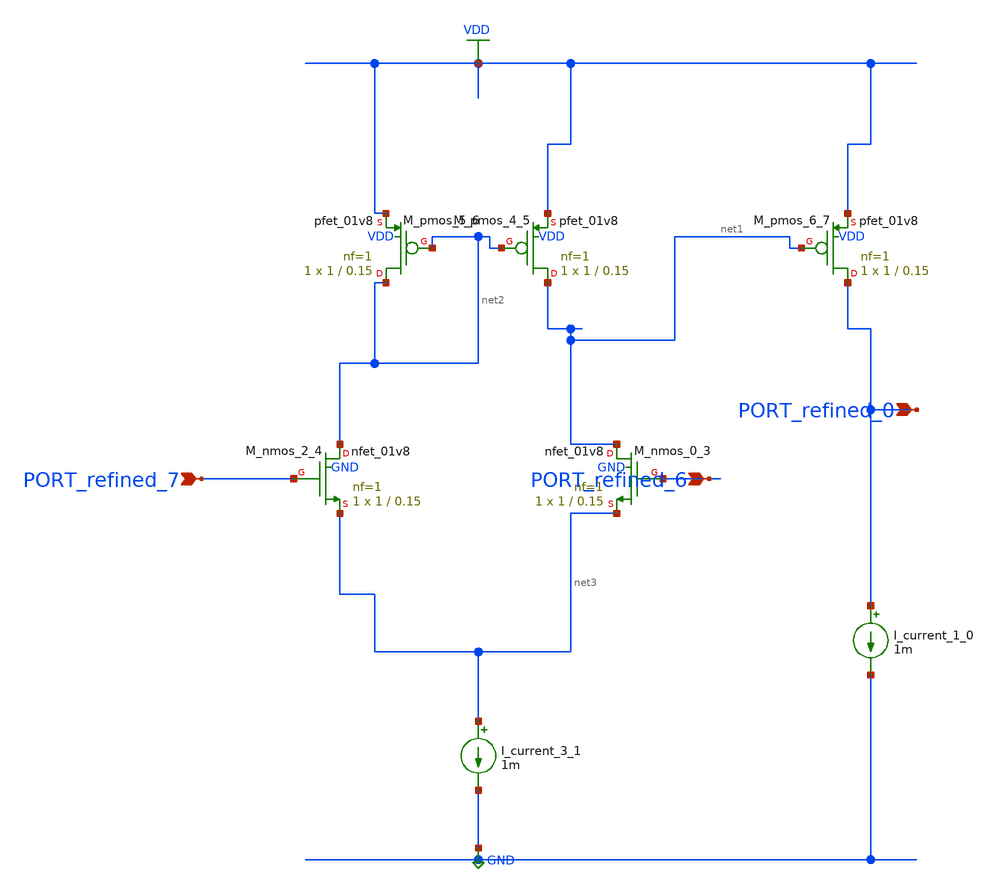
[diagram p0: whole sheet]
** sch_path: schematics/Image2Net/112.sch
**.subckt 112 PORT_refined_0 PORT_refined_6 PORT_refined_7
*.ipin PORT_refined_0
*.ipin PORT_refined_6
*.ipin PORT_refined_7
I_current_1_0 PORT_refined_0 GND 1m
I_current_3_1 net3 GND 1m
XM_nmos_0_3 net1 PORT_refined_6 net3 GND sky130_fd_pr__nfet_01v8 L=0.15 W=1 nf=1 ad='int((1 + 1)/2) * 1 / 1 * 0.29'
+ as='int((1 + 2)/2) * 1 / 1 * 0.29' pd='2*int((1 + 1)/2) * (1 / 1 + 0.29)' ps='2*int((1 + 2)/2) * (1 / 1 + 0.29)'
+ nrd='0.29 / 1 ' nrs='0.29 / 1 ' sa=0 sb=0 sd=0 mult=1 m=1
XM_nmos_2_4 net2 PORT_refined_7 net3 GND sky130_fd_pr__nfet_01v8 L=0.15 W=1 nf=1 ad='int((1 + 1)/2) * 1 / 1 * 0.29'
+ as='int((1 + 2)/2) * 1 / 1 * 0.29' pd='2*int((1 + 1)/2) * (1 / 1 + 0.29)' ps='2*int((1 + 2)/2) * (1 / 1 + 0.29)'
+ nrd='0.29 / 1 ' nrs='0.29 / 1 ' sa=0 sb=0 sd=0 mult=1 m=1
XM_pmos_4_5 net1 net2 VDD VDD sky130_fd_pr__pfet_01v8 L=0.15 W=1 nf=1 ad='int((1 + 1)/2) * 1 / 1 * 0.29'
+ as='int((1 + 2)/2) * 1 / 1 * 0.29' pd='2*int((1 + 1)/2) * (1 / 1 + 0.29)' ps='2*int((1 + 2)/2) * (1 / 1 + 0.29)'
+ nrd='0.29 / 1 ' nrs='0.29 / 1 ' sa=0 sb=0 sd=0 mult=1 m=1
XM_pmos_5_6 net2 net2 VDD VDD sky130_fd_pr__pfet_01v8 L=0.15 W=1 nf=1 ad='int((1 + 1)/2) * 1 / 1 * 0.29'
+ as='int((1 + 2)/2) * 1 / 1 * 0.29' pd='2*int((1 + 1)/2) * (1 / 1 + 0.29)' ps='2*int((1 + 2)/2) * (1 / 1 + 0.29)'
+ nrd='0.29 / 1 ' nrs='0.29 / 1 ' sa=0 sb=0 sd=0 mult=1 m=1
XM_pmos_6_7 PORT_refined_0 net1 VDD VDD sky130_fd_pr__pfet_01v8 L=0.15 W=1 nf=1 ad='int((1 + 1)/2) * 1 / 1 * 0.29'
+ as='int((1 + 2)/2) * 1 / 1 * 0.29' pd='2*int((1 + 1)/2) * (1 / 1 + 0.29)' ps='2*int((1 + 2)/2) * (1 / 1 + 0.29)'
+ nrd='0.29 / 1 ' nrs='0.29 / 1 ' sa=0 sb=0 sd=0 mult=1 m=1
**.ends
.GLOBAL GND
.GLOBAL VDD
.end
